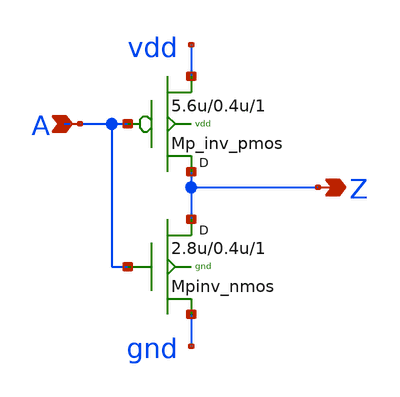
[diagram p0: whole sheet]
** sch_path: sram_2_64_scn4m_lcc/pinv_8.sch
**.subckt pinv_8 A Z
*.ipin A
*.opin Z
Mpinv_nmos Z A gnd gnd n w=2.8u l=0.4u m=1
Mp_inv_pmos Z A vdd vdd p w=5.6u l=0.4u m=1
**.ends
.end
